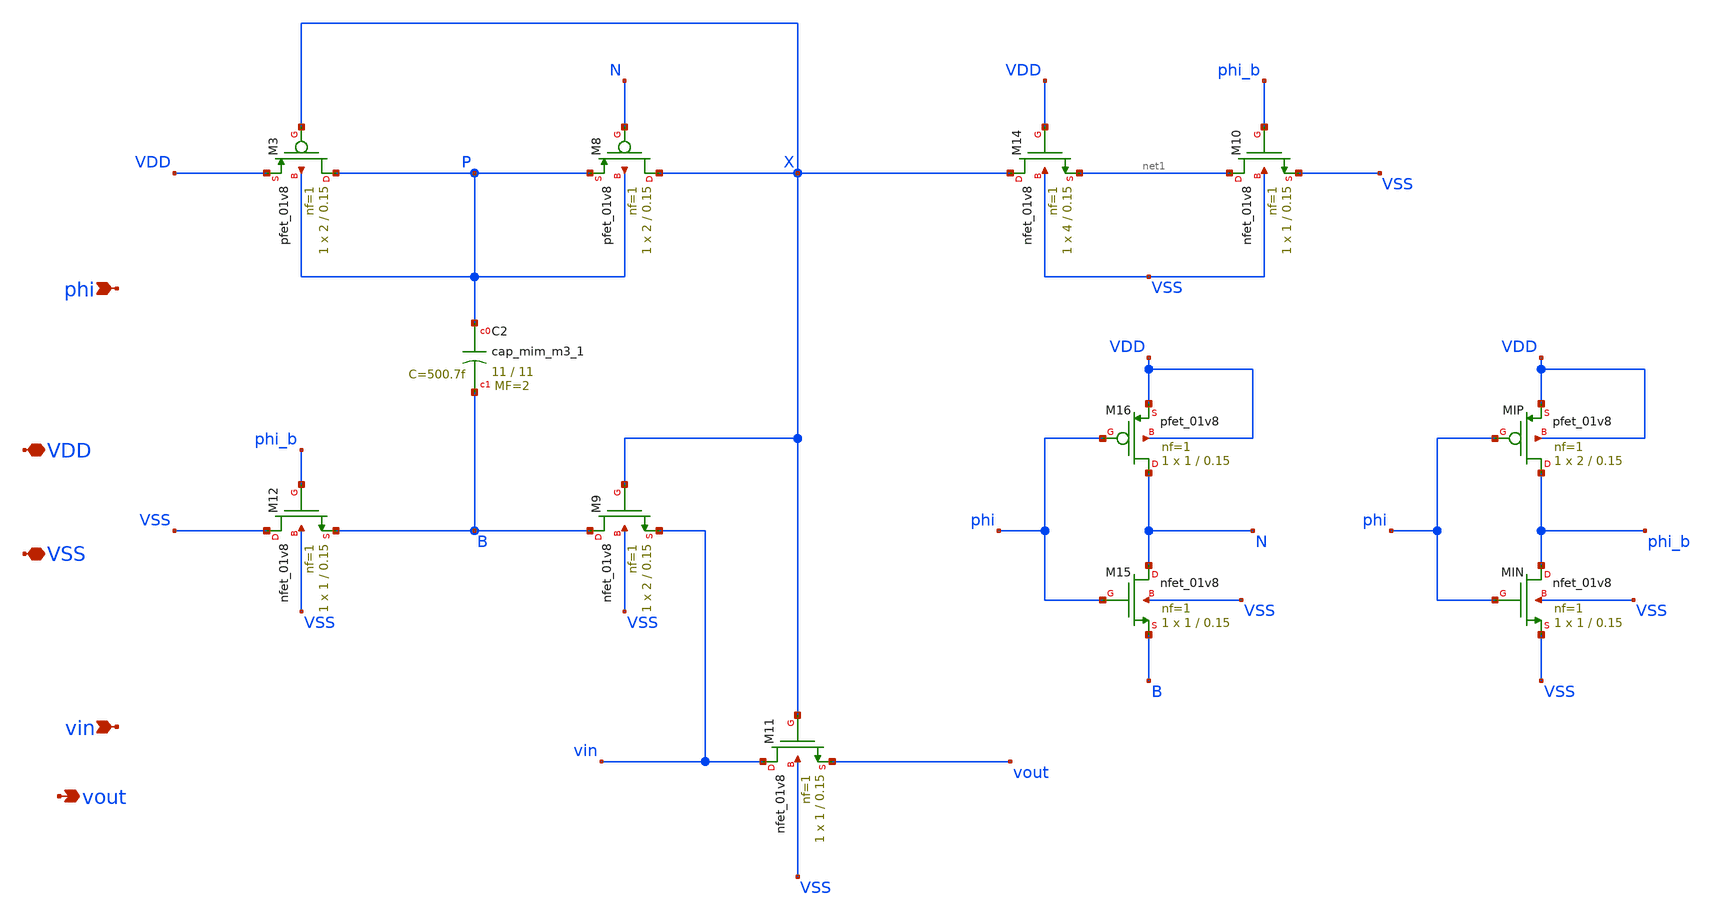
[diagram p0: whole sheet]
** sch_path: xschem/bootstrap_switch.sch
**.subckt bootstrap_switch VDD VSS vout phi vin
*.iopin VDD
*.iopin VSS
*.opin vout
*.ipin phi
*.ipin vin
XM8 X N P P sky130_fd_pr__pfet_01v8 L=0.15 W=2 nf=1 ad='int((1 + 1)/2) * 2 / 1 * 0.29' as='int((1 + 2)/2) * 2 / 1 * 0.29'
+ pd='2*int((1 + 1)/2) * (2 / 1 + 0.29)' ps='2*int((1 + 2)/2) * (2 / 1 + 0.29)' nrd='0.29 / 2 ' nrs='0.29 / 2 '
+ sa=0 sb=0 sd=0 mult=1 m=1
XM11 vin X vout VSS sky130_fd_pr__nfet_01v8 L=0.15 W=1 nf=1 ad='int((1 + 1)/2) * 1 / 1 * 0.29' as='int((1 + 2)/2) * 1 / 1 * 0.29'
+ pd='2*int((1 + 1)/2) * (1 / 1 + 0.29)' ps='2*int((1 + 2)/2) * (1 / 1 + 0.29)' nrd='0.29 / 1 ' nrs='0.29 / 1 '
+ sa=0 sb=0 sd=0 mult=1 m=1
XC2 P B sky130_fd_pr__cap_mim_m3_1 W=11 L=11 MF=2 m=2
XM9 B X vin VSS sky130_fd_pr__nfet_01v8 L=0.15 W=2 nf=1 ad='int((1 + 1)/2) * 2 / 1 * 0.29' as='int((1 + 2)/2) * 2 / 1 * 0.29'
+ pd='2*int((1 + 1)/2) * (2 / 1 + 0.29)' ps='2*int((1 + 2)/2) * (2 / 1 + 0.29)' nrd='0.29 / 2 ' nrs='0.29 / 2 '
+ sa=0 sb=0 sd=0 mult=1 m=1
XM12 VSS phi_b B VSS sky130_fd_pr__nfet_01v8 L=0.15 W=1 nf=1 ad='int((1 + 1)/2) * 1 / 1 * 0.29' as='int((1 + 2)/2) * 1 / 1 * 0.29'
+ pd='2*int((1 + 1)/2) * (1 / 1 + 0.29)' ps='2*int((1 + 2)/2) * (1 / 1 + 0.29)' nrd='0.29 / 1 ' nrs='0.29 / 1 '
+ sa=0 sb=0 sd=0 mult=1 m=1
XM14 X VDD net1 VSS sky130_fd_pr__nfet_01v8 L=0.15 W=4 nf=1 ad='int((1 + 1)/2) * 4 / 1 * 0.29' as='int((1 + 2)/2) * 4 / 1 * 0.29'
+ pd='2*int((1 + 1)/2) * (4 / 1 + 0.29)' ps='2*int((1 + 2)/2) * (4 / 1 + 0.29)' nrd='0.29 / 4 ' nrs='0.29 / 4 '
+ sa=0 sb=0 sd=0 mult=1 m=1
XM3 P X VDD P sky130_fd_pr__pfet_01v8 L=0.15 W=2 nf=1 ad='int((1 + 1)/2) * 2 / 1 * 0.29' as='int((1 + 2)/2) * 2 / 1 * 0.29'
+ pd='2*int((1 + 1)/2) * (2 / 1 + 0.29)' ps='2*int((1 + 2)/2) * (2 / 1 + 0.29)' nrd='0.29 / 2 ' nrs='0.29 / 2 '
+ sa=0 sb=0 sd=0 mult=1 m=1
XM10 net1 phi_b VSS VSS sky130_fd_pr__nfet_01v8 L=0.15 W=1 nf=1 ad='int((1 + 1)/2) * 1 / 1 * 0.29' as='int((1 + 2)/2) * 1 / 1 * 0.29'
+ pd='2*int((1 + 1)/2) * (1 / 1 + 0.29)' ps='2*int((1 + 2)/2) * (1 / 1 + 0.29)' nrd='0.29 / 1 ' nrs='0.29 / 1 '
+ sa=0 sb=0 sd=0 mult=1 m=1
XM15 N phi B VSS sky130_fd_pr__nfet_01v8 L=0.15 W=1 nf=1 ad='int((1 + 1)/2) * 1 / 1 * 0.29' as='int((1 + 2)/2) * 1 / 1 * 0.29'
+ pd='2*int((1 + 1)/2) * (1 / 1 + 0.29)' ps='2*int((1 + 2)/2) * (1 / 1 + 0.29)' nrd='0.29 / 1 ' nrs='0.29 / 1 '
+ sa=0 sb=0 sd=0 mult=1 m=1
XM16 N phi VDD VDD sky130_fd_pr__pfet_01v8 L=0.15 W=1 nf=1 ad='int((1 + 1)/2) * 1 / 1 * 0.29' as='int((1 + 2)/2) * 1 / 1 * 0.29'
+ pd='2*int((1 + 1)/2) * (1 / 1 + 0.29)' ps='2*int((1 + 2)/2) * (1 / 1 + 0.29)' nrd='0.29 / 1 ' nrs='0.29 / 1 '
+ sa=0 sb=0 sd=0 mult=1 m=1
XMIN phi_b phi VSS VSS sky130_fd_pr__nfet_01v8 L=0.15 W=1 nf=1 ad='int((1 + 1)/2) * 1 / 1 * 0.29' as='int((1 + 2)/2) * 1 / 1 * 0.29'
+ pd='2*int((1 + 1)/2) * (1 / 1 + 0.29)' ps='2*int((1 + 2)/2) * (1 / 1 + 0.29)' nrd='0.29 / 1 ' nrs='0.29 / 1 '
+ sa=0 sb=0 sd=0 mult=1 m=1
XMIP phi_b phi VDD VDD sky130_fd_pr__pfet_01v8 L=0.15 W=2 nf=1 ad='int((1 + 1)/2) * 2 / 1 * 0.29' as='int((1 + 2)/2) * 2 / 1 * 0.29'
+ pd='2*int((1 + 1)/2) * (2 / 1 + 0.29)' ps='2*int((1 + 2)/2) * (2 / 1 + 0.29)' nrd='0.29 / 2 ' nrs='0.29 / 2 '
+ sa=0 sb=0 sd=0 mult=1 m=1
**.ends
.end
